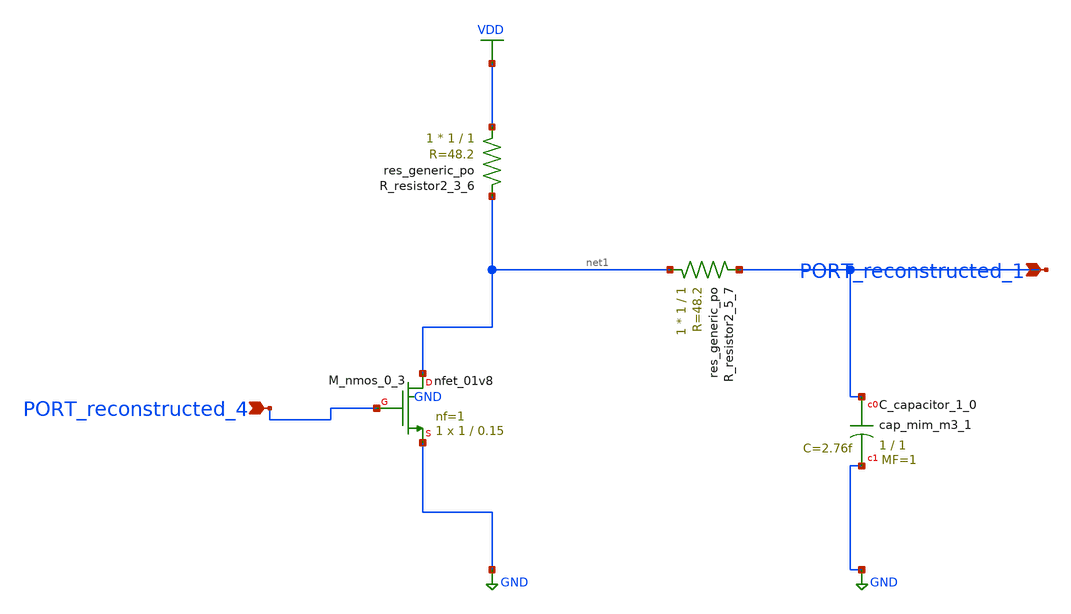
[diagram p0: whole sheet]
** sch_path: schematics/AMSNet/533.sch
**.subckt 533 PORT_reconstructed_4 PORT_reconstructed_1
*.ipin PORT_reconstructed_4
*.ipin PORT_reconstructed_1
XC_capacitor_1_0 PORT_reconstructed_1 GND sky130_fd_pr__cap_mim_m3_1 W=1 L=1 MF=1 m=1
XM_nmos_0_3 net1 PORT_reconstructed_4 GND GND sky130_fd_pr__nfet_01v8 L=0.15 W=1 nf=1 ad='int((1 + 1)/2) * 1 / 1 * 0.29'
+ as='int((1 + 2)/2) * 1 / 1 * 0.29' pd='2*int((1 + 1)/2) * (1 / 1 + 0.29)' ps='2*int((1 + 2)/2) * (1 / 1 + 0.29)'
+ nrd='0.29 / 1 ' nrs='0.29 / 1 ' sa=0 sb=0 sd=0 mult=1 m=1
XR_resistor2_3_6 VDD net1 sky130_fd_pr__res_generic_po W=1 L=1 m=1
XR_resistor2_5_7 net1 PORT_reconstructed_1 sky130_fd_pr__res_generic_po W=1 L=1 m=1
**.ends
.GLOBAL GND
.GLOBAL VDD
.end
